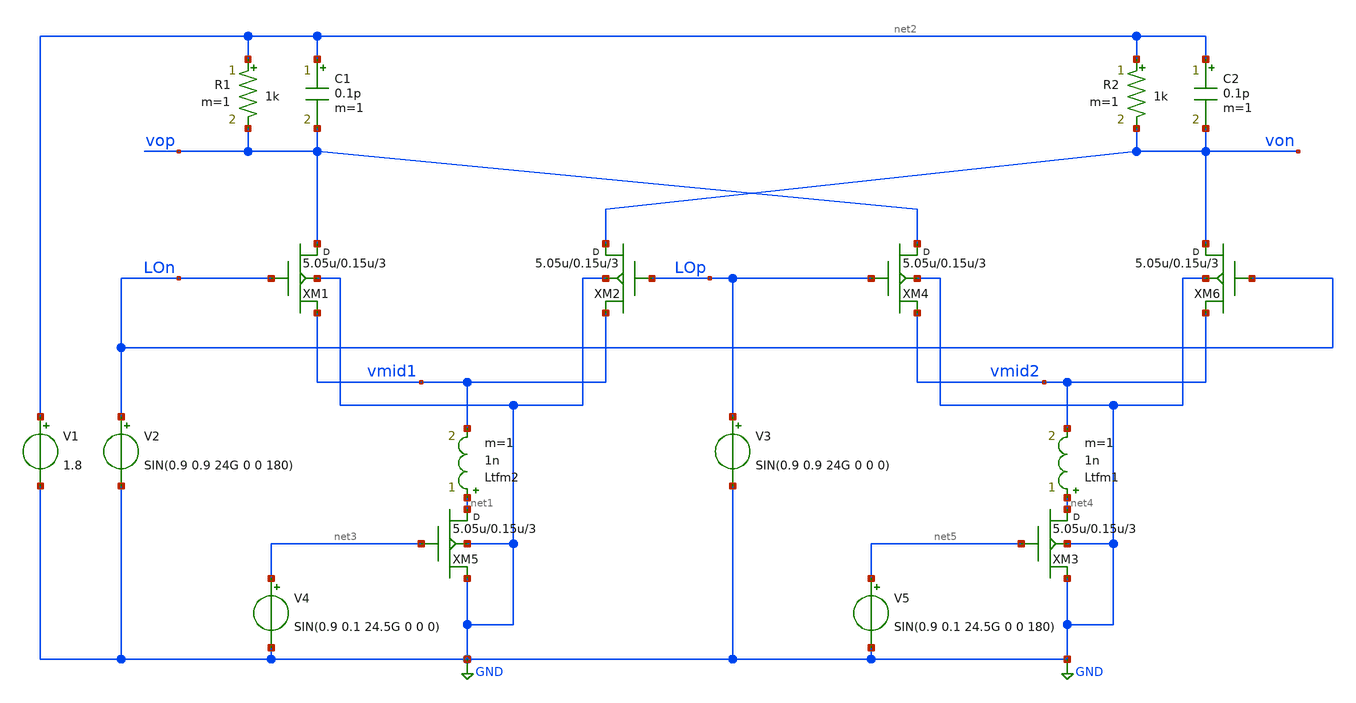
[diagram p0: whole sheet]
** sch_path: xschem/MIXER_24G.sch
**.subckt MIXER_24G
XM5 net1 net3 GND GND sky130_fd_pr__rf_nfet_01v8_bM04W5p00L0p15_ext w=5.05u l=0.15u m=3
XM1 vop LOn vmid1 GND sky130_fd_pr__rf_nfet_01v8_bM04W5p00L0p15_ext w=5.05u l=0.15u m=3
XM2 von LOp vmid1 GND sky130_fd_pr__rf_nfet_01v8_bM04W5p00L0p15_ext w=5.05u l=0.15u m=3
Ltfm2 net1 vmid1 1n m=1
C1 net2 vop 0.1p m=1
R1 net2 vop 1k m=1
C2 net2 von 0.1p m=1
R2 net2 von 1k m=1
V1 net2 GND 1.8
V2 LOn GND SIN(0.9 0.9 24G 0 0 180)
V3 LOp GND SIN(0.9 0.9 24G 0 0 0)
V4 net3 GND SIN(0.9 0.1 24.5G 0 0 0)
XM3 net4 net5 GND GND sky130_fd_pr__rf_nfet_01v8_bM04W5p00L0p15_ext w=5.05u l=0.15u m=3
XM4 vop LOp vmid2 GND sky130_fd_pr__rf_nfet_01v8_bM04W5p00L0p15_ext w=5.05u l=0.15u m=3
XM6 von LOn vmid2 GND sky130_fd_pr__rf_nfet_01v8_bM04W5p00L0p15_ext w=5.05u l=0.15u m=3
Ltfm1 net4 vmid2 1n m=1
V5 net5 GND SIN(0.9 0.1 24.5G 0 0 180)
**** begin user architecture code


.subckt sky130_fd_pr__rf_nfet_01v8_bM04W5p00L0p15_ext DRAIN GATE SOURCE SUBSTRATE
X0 DRAIN GATE SOURCE SUBSTRATE sky130_fd_pr__nfet_01v8 ad=2.828e+12p pd=2.132e+07u as=4.242e+12p
+ ps=3.198e+07u w=5.05e+06u l=150000u
X1 SOURCE SUBSTRATE SUBSTRATE SUBSTRATE sky130_fd_pr__nfet_01v8 ad=0p pd=0u as=3.03e+12p
+ ps=2.14e+07u w=5.05e+06u l=150000u
X2 SOURCE GATE DRAIN SUBSTRATE sky130_fd_pr__nfet_01v8 ad=0p pd=0u as=0p ps=0u w=5.05e+06u l=150000u
X3 DRAIN GATE SOURCE SUBSTRATE sky130_fd_pr__nfet_01v8 ad=0p pd=0u as=0p ps=0u w=5.05e+06u l=150000u
X4 SUBSTRATE SUBSTRATE SOURCE SUBSTRATE sky130_fd_pr__nfet_01v8 ad=0p pd=0u as=0p ps=0u w=5.05e+06u
+ l=150000u
X5 SOURCE GATE DRAIN SUBSTRATE sky130_fd_pr__nfet_01v8 ad=0p pd=0u as=0p ps=0u w=5.05e+06u l=150000u
.ends
.options savecurrents
.tran 0.05ps 20ns
.control
run
display
plot v(von) v(vop)

.endc


.lib $::SKYWATER_MODELS/sky130.lib.spice ss
* .include $::PDKPATH/libs.ref/sky130_fd_sc_hvl/spice/sky130_fd_sc_hvl.spice

**** end user architecture code
**.ends
.GLOBAL GND
.end
